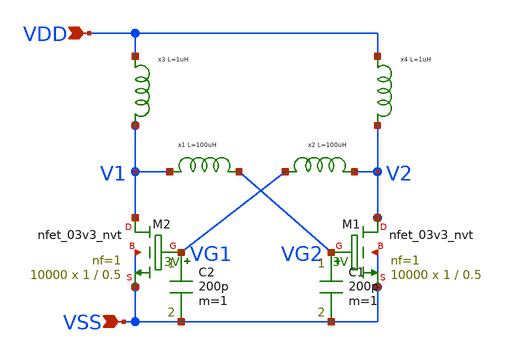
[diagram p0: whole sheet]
** sch_path: design/LELO_SVOD_SKY130A/LELO_EXSC.sch
**.subckt LELO_EXSC VSS VDD
*.ipin VSS
*.ipin VDD
x1 V1 VG2 MLF2012C101KT000_p
x2 V2 VG1 MLF2012C101KT000_p
x3 VDD V1 MLF2012A1R0JT000_p
x4 VDD V2 MLF2012A1R0JT000_p
C1 VG2 VSS 200p m=1
C2 VG1 VSS 200p m=1
XM2 V1 VG1 VSS VSS sky130_fd_pr__nfet_03v3_nvt L=0.5 W=1 nf=1 ad='int((1 + 1)/2) * 1 / 1 * 0.29' as='int((1 + 2)/2) * 1 / 1 * 0.29'
+ pd='2*int((1 + 1)/2) * (1 / 1 + 0.29)' ps='2*int((1 + 2)/2) * (1 / 1 + 0.29)' nrd='0.29 / 1 ' nrs='0.29 / 1 '
+ sa=0 sb=0 sd=0 mult=10000 m=10000
XM1 V2 VG2 VSS VSS sky130_fd_pr__nfet_03v3_nvt L=0.5 W=1 nf=1 ad='int((1 + 1)/2) * 1 / 1 * 0.29' as='int((1 + 2)/2) * 1 / 1 * 0.29'
+ pd='2*int((1 + 1)/2) * (1 / 1 + 0.29)' ps='2*int((1 + 2)/2) * (1 / 1 + 0.29)' nrd='0.29 / 1 ' nrs='0.29 / 1 '
+ sa=0 sb=0 sd=0 mult=10000 m=10000
**.ends

* expanding   symbol:  LELO_SVOD_SKY130A/MLF2012C101KT000_p.sym # of pins=2
** sym_path: design/LELO_SVOD_SKY130A/MLF2012C101KT000_p.sym
.SUBCKT MLF2012C101KT000_p n1 n2
C1 13 17 2.53913456E-12
C2 n1 18 1.59562912E-12
L1 n1 11 1.71914388E-07
L2 11 12 1.82626669E-05
L3 12 13 7.93253796E-05
L4 12 17 4.49576054E-04
L5 13 14 6.53075255E-07
L6 14 15 1.51947035E-06
L7 15 16 4.33477754E-06
R1 11 12 8.80004396E+03
R2 12 13 4.43326588E+04
R3 12 17 9.30797466E+03
R4 n2 13 3.96223318E+01
R5 n2 14 1.93379287E+01
R6 n2 15 9.43799798E+00
R7 n2 16 4.60627439E+00
R8 n2 18 2.00000000E+01
R9 n1 n2 1.00000000E+09
.ENDS MLF2012C101KT000_p

* expanding   symbol:  LELO_SVOD_SKY130A/MLF2012A1R0JT000_p.sym # of pins=2
** sym_path: design/LELO_SVOD_SKY130A/MLF2012A1R0JT000_p.sym
.SUBCKT MLF2012A1R0JT000_p n1 n2
C1 13 17 4.51173927E-12
C2 n1 18 9.42055438E-13
L1 n1 11 1.22046627E-08
L2 11 12 1.81373699E-07
L3 12 13 7.83278932E-07
L4 12 17 3.34324717E-06
L5 13 14 7.78598512E-09
L6 14 15 1.81151766E-08
L7 15 16 5.16793633E-08
R1 11 12 4.74034174E+02
R2 12 13 8.06355781E+05
R3 12 17 6.05296016E+02
R4 n2 13 2.37733991E+00
R5 n2 14 1.16027572E+00
R6 n2 15 5.66279879E-01
R7 n2 16 2.76376463E-01
R8 n2 18 2.00000000E+01
R9 n1 n2 1.00000000E+09
.ENDS MLF2012A1R0JT000_p
.end
